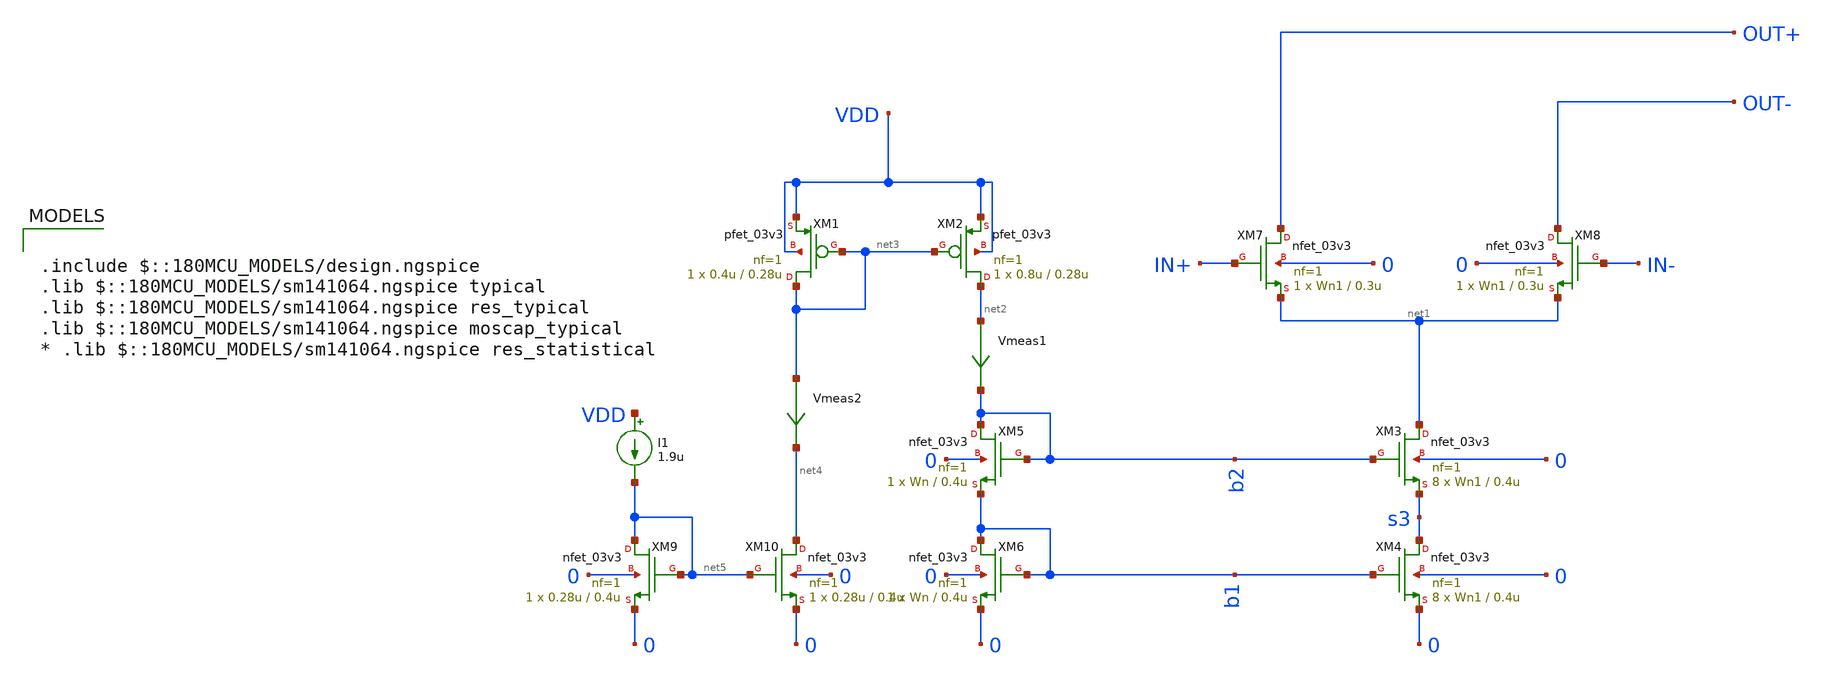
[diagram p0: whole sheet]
** sch_path: DAC/xschem/analog_cell/test/test)current_unit.sch
**.subckt test)current_unit
XM3 net1 b2 s3 0 nfet_03v3 L=0.4u W=Wn1 nf=1 ad='int((nf+1)/2) * W/nf * 0.18u' as='int((nf+2)/2) * W/nf * 0.18u'
+ pd='2*int((nf+1)/2) * (W/nf + 0.18u)' ps='2*int((nf+2)/2) * (W/nf + 0.18u)' nrd='0.18u / W' nrs='0.18u / W'
+ sa=0 sb=0 sd=0 m=8
XM4 s3 b1 0 0 nfet_03v3 L=0.4u W=Wn1 nf=1 ad='int((nf+1)/2) * W/nf * 0.18u' as='int((nf+2)/2) * W/nf * 0.18u'
+ pd='2*int((nf+1)/2) * (W/nf + 0.18u)' ps='2*int((nf+2)/2) * (W/nf + 0.18u)' nrd='0.18u / W' nrs='0.18u / W'
+ sa=0 sb=0 sd=0 m=8
XM5 b2 b2 b1 0 nfet_03v3 L=0.4u W=Wn nf=1 ad='int((nf+1)/2) * W/nf * 0.18u' as='int((nf+2)/2) * W/nf * 0.18u'
+ pd='2*int((nf+1)/2) * (W/nf + 0.18u)' ps='2*int((nf+2)/2) * (W/nf + 0.18u)' nrd='0.18u / W' nrs='0.18u / W'
+ sa=0 sb=0 sd=0 m=1
XM6 b1 b1 0 0 nfet_03v3 L=0.4u W=Wn nf=1 ad='int((nf+1)/2) * W/nf * 0.18u' as='int((nf+2)/2) * W/nf * 0.18u'
+ pd='2*int((nf+1)/2) * (W/nf + 0.18u)' ps='2*int((nf+2)/2) * (W/nf + 0.18u)' nrd='0.18u / W' nrs='0.18u / W'
+ sa=0 sb=0 sd=0 m=1
Vmeas1 net2 b2 0
.save i(vmeas1)
XM1 net3 net3 VDD VDD pfet_03v3 L=0.28u W=0.4u nf=1 ad='int((nf+1)/2) * W/nf * 0.18u' as='int((nf+2)/2) * W/nf * 0.18u'
+ pd='2*int((nf+1)/2) * (W/nf + 0.18u)' ps='2*int((nf+2)/2) * (W/nf + 0.18u)' nrd='0.18u / W' nrs='0.18u / W'
+ sa=0 sb=0 sd=0 m=1
XM2 net2 net3 VDD VDD pfet_03v3 L=0.28u W=0.8u nf=1 ad='int((nf+1)/2) * W/nf * 0.18u' as='int((nf+2)/2) * W/nf * 0.18u'
+ pd='2*int((nf+1)/2) * (W/nf + 0.18u)' ps='2*int((nf+2)/2) * (W/nf + 0.18u)' nrd='0.18u / W' nrs='0.18u / W'
+ sa=0 sb=0 sd=0 m=1
XM7 OUT+ IN+ net1 0 nfet_03v3 L=0.3u W=Wn1 nf=1 ad='int((nf+1)/2) * W/nf * 0.18u' as='int((nf+2)/2) * W/nf * 0.18u'
+ pd='2*int((nf+1)/2) * (W/nf + 0.18u)' ps='2*int((nf+2)/2) * (W/nf + 0.18u)' nrd='0.18u / W' nrs='0.18u / W'
+ sa=0 sb=0 sd=0 m=1
XM8 OUT- IN- net1 0 nfet_03v3 L=0.3u W=Wn1 nf=1 ad='int((nf+1)/2) * W/nf * 0.18u' as='int((nf+2)/2) * W/nf * 0.18u'
+ pd='2*int((nf+1)/2) * (W/nf + 0.18u)' ps='2*int((nf+2)/2) * (W/nf + 0.18u)' nrd='0.18u / W' nrs='0.18u / W'
+ sa=0 sb=0 sd=0 m=1
I1 VDD net5 1.9u
Vmeas2 net3 net4 0
.save i(vmeas2)
XM9 net5 net5 0 0 nfet_03v3 L=0.4u W=0.28u nf=1 ad='int((nf+1)/2) * W/nf * 0.18u' as='int((nf+2)/2) * W/nf * 0.18u'
+ pd='2*int((nf+1)/2) * (W/nf + 0.18u)' ps='2*int((nf+2)/2) * (W/nf + 0.18u)' nrd='0.18u / W' nrs='0.18u / W'
+ sa=0 sb=0 sd=0 m=1
XM10 net4 net5 0 0 nfet_03v3 L=0.4u W=0.28u nf=1 ad='int((nf+1)/2) * W/nf * 0.18u' as='int((nf+2)/2) * W/nf * 0.18u'
+ pd='2*int((nf+1)/2) * (W/nf + 0.18u)' ps='2*int((nf+2)/2) * (W/nf + 0.18u)' nrd='0.18u / W' nrs='0.18u / W'
+ sa=0 sb=0 sd=0 m=1
**** begin user architecture code

.include $::180MCU_MODELS/design.ngspice
.lib $::180MCU_MODELS/sm141064.ngspice typical
.lib $::180MCU_MODELS/sm141064.ngspice res_typical
.lib $::180MCU_MODELS/sm141064.ngspice moscap_typical
* .lib $::180MCU_MODELS/sm141064.ngspice res_statistical



V0 VDD 0 3
V1 IN+ 0 3
V2 IN- 0 0

.options savecurrents
.param Wn=0.3u
.param Wn1=0.3u
.control
	dc I0 1u 4u 0.1u
	plot v(d3)
	plot i(Vmeas1) i(Vmeas2)
	*tran 1u 100u
 	plot v(b2)-v(s3)-@m.xm3.m0[vth]
	plot v(b1)-@m.xm4.m0[vth]
	plot @m.xm3.m0[vth]
	plot @m.xm4.m0[vth]
.endc

.save all @m.xm1.m0[vth] @m.xm2.m0[vth] @m.xm3.m0[vth] @m.xm4.m0[vth]


**** end user architecture code
**.ends
.end
